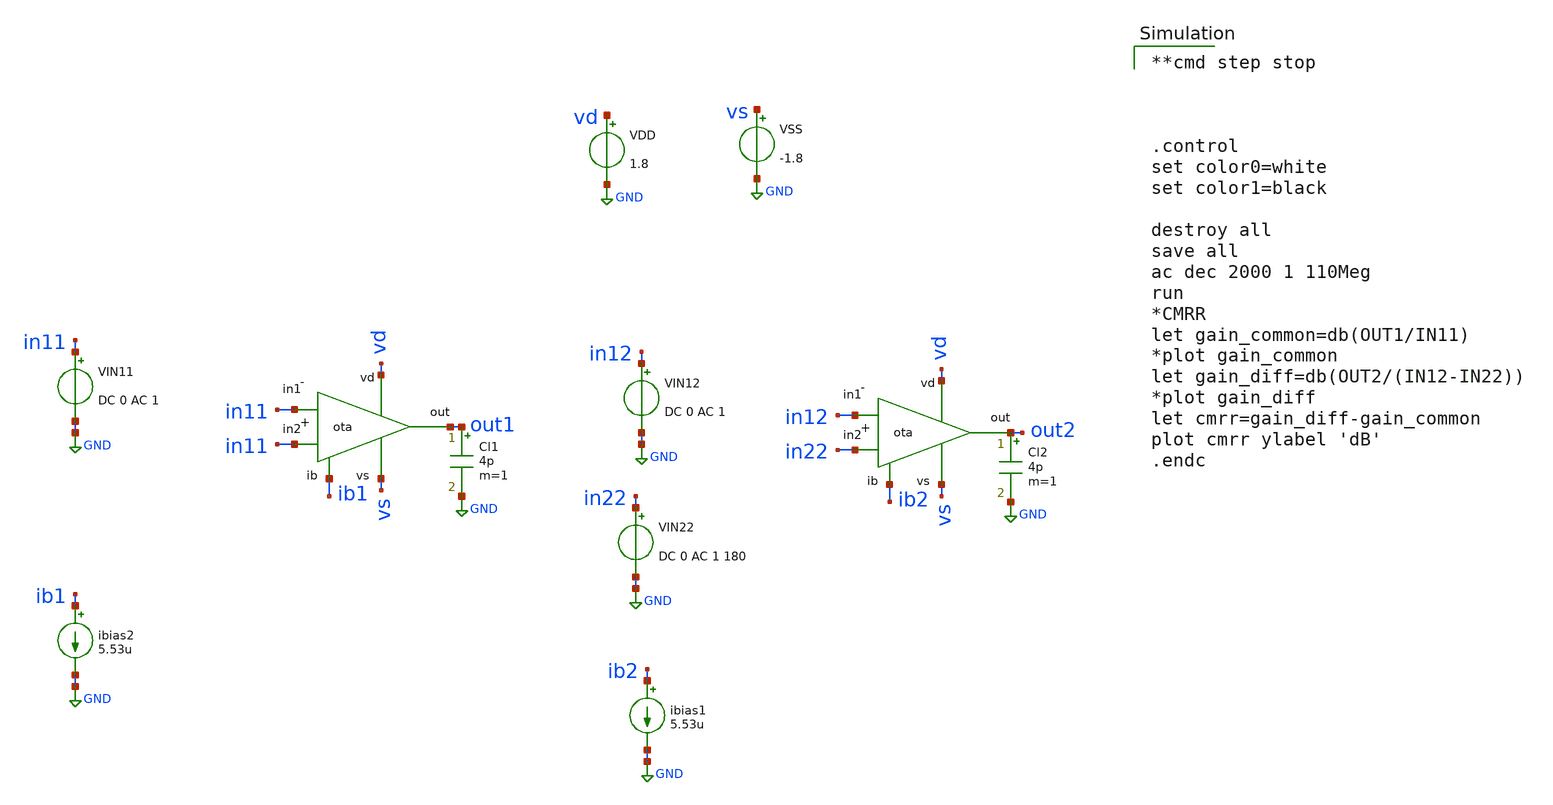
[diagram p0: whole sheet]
** sch_path: amp-op/xschem/ota_tb-CMRR.sch
* Copyright 2020 Stefan Frederik Schippers
* Licensed under the Apache License, Version 2.0 (the "License");
* you may not use this file except in compliance with the License.
* You may obtain a copy of the License at
* https://www.apache.org/licenses/LICENSE-2.0
* Unless required by applicable law or agreed to in writing, software
* distributed under the License is distributed on an "AS IS" BASIS,
* WITHOUT WARRANTIES OR CONDITIONS OF ANY KIND, either express or implied.
* See the License for the specific language governing permissions and
* limitations under the License.
**.subckt ota_tb-CMRR
VIN11 in11 GND DC 0 AC 1
ibias2 ib1 GND 5.53u
VDD vd GND 1.8
VSS vs GND -1.8
VIN12 in12 GND DC 0 AC 1
ibias1 ib2 GND 5.53u
VIN22 in22 GND DC 0 AC 1 180
Cl1 out1 GND 4p m=1
Cl2 out2 GND 4p m=1
X1 vd ib1 out1 in11 in11 vs ota
X2 vd ib2 out2 in22 in12 vs ota
**** begin user architecture code

**cmd step stop



.control
set color0=white
set color1=black

destroy all
save all
ac dec 2000 1 110Meg
run
*CMRR
let gain_common=db(OUT1/IN11)
*plot gain_common
let gain_diff=db(OUT2/(IN12-IN22))
*plot gain_diff
let cmrr=gain_diff-gain_common
plot cmrr ylabel 'dB'
.endc

 .lib $::SKYWATER_MODELS/sky130.lib.spice tt
.include $::SKYWATER_STDCELLS/sky130_fd_sc_hd.spice

**** end user architecture code
**.ends

* expanding   symbol:  /home/hugodg/projects-sky130/temp-sensor/amp-op/xschem/ota.sym # of pins=6
** sym_path: amp-op/xschem/ota.sym
** sch_path: amp-op/xschem/ota.sch
.subckt ota vd ib out in2 in1 vs
*.iopin vd
*.iopin vs
*.iopin ib
*.ipin in1
*.ipin in2
*.opin out
XCC out d sky130_fd_pr__cap_mim_m3_1 W=21 L=21 MF=1 m=1
XM5 ib ib vd vd sky130_fd_pr__pfet_01v8 L=1 W=6 nf=1 ad='int((nf+1)/2) * W/nf * 0.29' as='int((nf+2)/2) * W/nf * 0.29'
+ pd='2*int((nf+1)/2) * (W/nf + 0.29)' ps='2*int((nf+2)/2) * (W/nf + 0.29)' nrd='0.29 / W' nrs='0.29 / W'
+ sa=0 sb=0 sd=0 mult=1 m=1
XM6 b ib vd vd sky130_fd_pr__pfet_01v8 L=1 W=6 nf=1 ad='int((nf+1)/2) * W/nf * 0.29' as='int((nf+2)/2) * W/nf * 0.29'
+ pd='2*int((nf+1)/2) * (W/nf + 0.29)' ps='2*int((nf+2)/2) * (W/nf + 0.29)' nrd='0.29 / W' nrs='0.29 / W'
+ sa=0 sb=0 sd=0 mult=1 m=1
XM8 out ib vd vd sky130_fd_pr__pfet_01v8 L=1 W=30 nf=4 ad='int((nf+1)/2) * W/nf * 0.29' as='int((nf+2)/2) * W/nf * 0.29'
+ pd='2*int((nf+1)/2) * (W/nf + 0.29)' ps='2*int((nf+2)/2) * (W/nf + 0.29)' nrd='0.29 / W' nrs='0.29 / W'
+ sa=0 sb=0 sd=0 mult=1 m=1
XM1 c in1 b b sky130_fd_pr__pfet_01v8 L=1 W=3 nf=1 ad='int((nf+1)/2) * W/nf * 0.29' as='int((nf+2)/2) * W/nf * 0.29'
+ pd='2*int((nf+1)/2) * (W/nf + 0.29)' ps='2*int((nf+2)/2) * (W/nf + 0.29)' nrd='0.29 / W' nrs='0.29 / W'
+ sa=0 sb=0 sd=0 mult=1 m=1
XM2 d in2 b b sky130_fd_pr__pfet_01v8 L=1 W=3 nf=1 ad='int((nf+1)/2) * W/nf * 0.29' as='int((nf+2)/2) * W/nf * 0.29'
+ pd='2*int((nf+1)/2) * (W/nf + 0.29)' ps='2*int((nf+2)/2) * (W/nf + 0.29)' nrd='0.29 / W' nrs='0.29 / W'
+ sa=0 sb=0 sd=0 mult=1 m=1
XM3 c c vs vs sky130_fd_pr__nfet_01v8 L=1 W=1 nf=1 ad='int((nf+1)/2) * W/nf * 0.29' as='int((nf+2)/2) * W/nf * 0.29'
+ pd='2*int((nf+1)/2) * (W/nf + 0.29)' ps='2*int((nf+2)/2) * (W/nf + 0.29)' nrd='0.29 / W' nrs='0.29 / W'
+ sa=0 sb=0 sd=0 mult=1 m=1
XM4 d c vs vs sky130_fd_pr__nfet_01v8 L=1 W=1 nf=1 ad='int((nf+1)/2) * W/nf * 0.29' as='int((nf+2)/2) * W/nf * 0.29'
+ pd='2*int((nf+1)/2) * (W/nf + 0.29)' ps='2*int((nf+2)/2) * (W/nf + 0.29)' nrd='0.29 / W' nrs='0.29 / W'
+ sa=0 sb=0 sd=0 mult=1 m=1
XM7 out d vs vs sky130_fd_pr__nfet_01v8 L=1 W=9 nf=2 ad='int((nf+1)/2) * W/nf * 0.29' as='int((nf+2)/2) * W/nf * 0.29'
+ pd='2*int((nf+1)/2) * (W/nf + 0.29)' ps='2*int((nf+2)/2) * (W/nf + 0.29)' nrd='0.29 / W' nrs='0.29 / W'
+ sa=0 sb=0 sd=0 mult=1 m=1
.ends

.GLOBAL GND
.end
